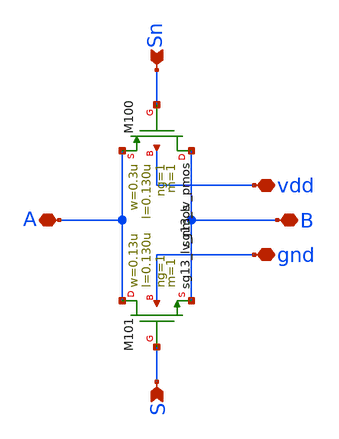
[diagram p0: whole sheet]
** sch_path: Enfoque_A/xschem/celdas/Ll.sch
**.subckt Ll gnd vdd B Sn S A
*.iopin gnd
*.iopin vdd
*.iopin B
*.ipin Sn
*.ipin S
*.iopin A
XM101 A S B gnd sg13_lv_nmos w=0.13u l=0.130u ng=1 m=1 mm_ok=1
XM100 B Sn A vdd sg13_lv_pmos w=0.3u l=0.130u ng=1 m=1 mm_ok=1
**.ends
.end
